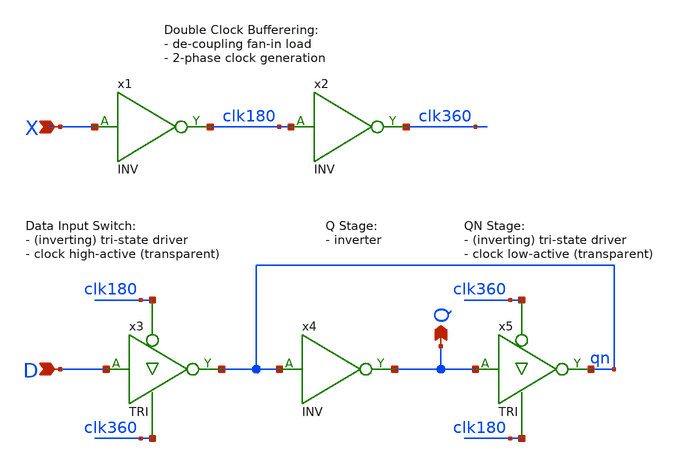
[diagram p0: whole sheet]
** sch_path: Sources/crafted/LATP.sch
**.subckt LATP X D Q
*.ipin X
*.ipin D
*.opin Q
x3 D clk180 clk360 qn VDD GND TRI Wmin=1.5u Lmin=1u g=2 m=1
x5 Q clk360 clk180 qn VDD GND TRI Wmin=1.5u Lmin=1u g=2 m=1
x1 X clk180 VDD GND INV Wmin=1.5u Lmin=1u g=2 m=1
x2 clk180 clk360 VDD GND INV Wmin=1.5u Lmin=1u g=2 m=1
x4 qn Q VDD GND INV Wmin=1.5u Lmin=1u g=2 m=1
**.ends
.end
